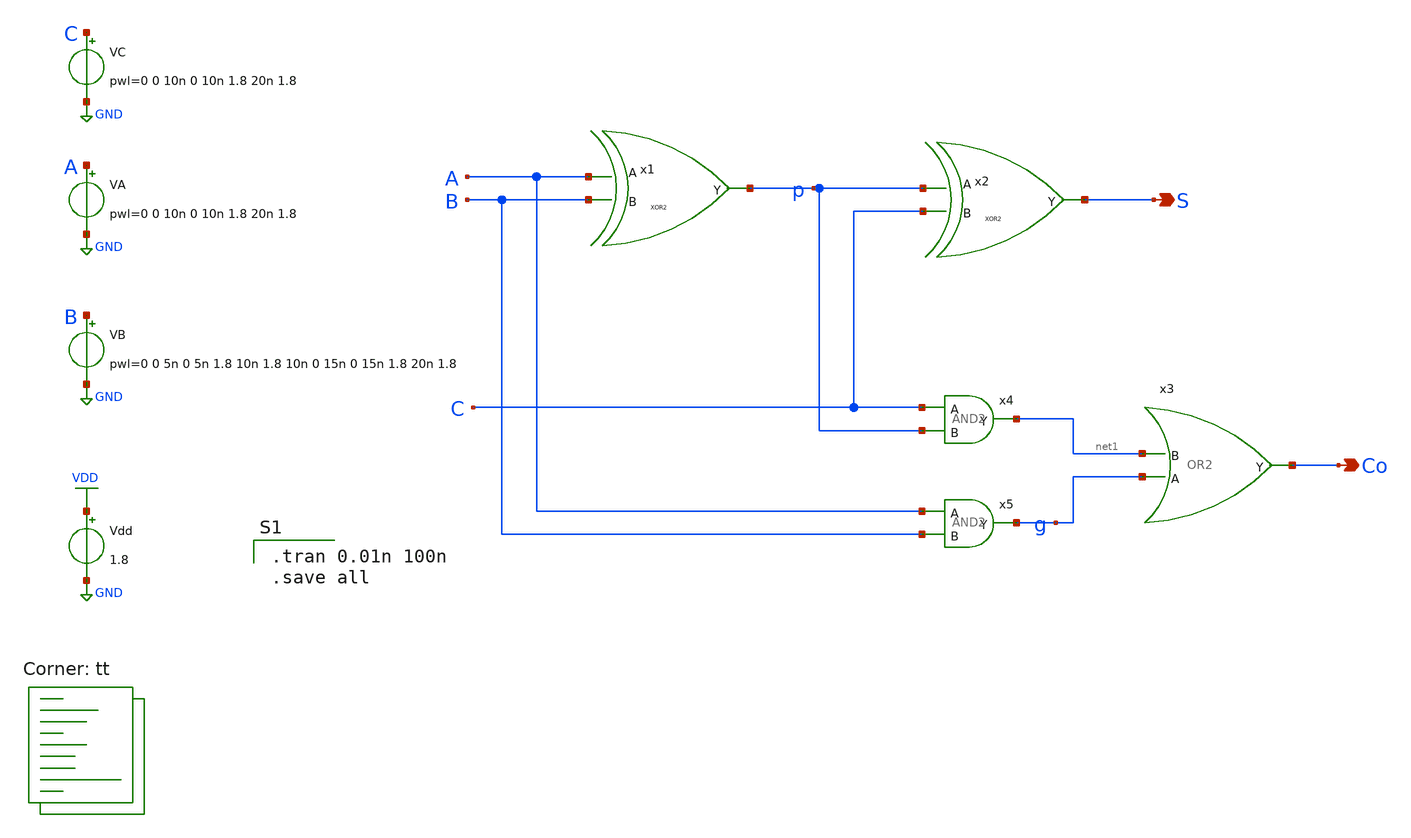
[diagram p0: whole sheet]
** sch_path: gates/FASIM.sch
**.subckt FASIM S Co
*.opin S
*.opin Co
x1 A B p XOR2
x2 p C S XOR2
x3 net1 Co g OR2
x4 C net1 p AND2
x5 A g B AND2
Vdd VDD GND 1.8
VA A GND pwl=0 0 10n 0 10n 1.8 20n 1.8
VB B GND pwl=0 0 5n 0 5n 1.8 10n 1.8 10n 0 15n 0 15n 1.8 20n 1.8
VC C GND pwl=0 0 10n 0 10n 1.8 20n 1.8
**** begin user architecture code

.tran 0.01n 100n
.save all

.lib $::SKYWATER_MODELS/sky130.lib.spice tt
**** end user architecture code
**.ends

* expanding   symbol:  XOR2.sym # of pins=3
** sym_path: gates/XOR2.sym
** sch_path: gates/XOR2.sch
.subckt XOR2 B A Y
*.ipin A
*.ipin B
*.opin Y
XM1 Y A net5 GND sky130_fd_pr__nfet_01v8 L=0.15 W=1 nf=1 ad='int((nf+1)/2) * W/nf * 0.29' as='int((nf+2)/2) * W/nf * 0.29'
+ pd='2*int((nf+1)/2) * (W/nf + 0.29)' ps='2*int((nf+2)/2) * (W/nf + 0.29)' nrd='0.29 / W' nrs='0.29 / W'
+ sa=0 sb=0 sd=0 mult=1 m=1
XM2 net5 B GND GND sky130_fd_pr__nfet_01v8 L=0.15 W=1 nf=1 ad='int((nf+1)/2) * W/nf * 0.29' as='int((nf+2)/2) * W/nf * 0.29'
+ pd='2*int((nf+1)/2) * (W/nf + 0.29)' ps='2*int((nf+2)/2) * (W/nf + 0.29)' nrd='0.29 / W' nrs='0.29 / W'
+ sa=0 sb=0 sd=0 mult=1 m=1
XM3 Y net1 net2 VDD sky130_fd_pr__pfet_01v8 L=0.15 W=1 nf=1 ad='int((nf+1)/2) * W/nf * 0.29' as='int((nf+2)/2) * W/nf * 0.29'
+ pd='2*int((nf+1)/2) * (W/nf + 0.29)' ps='2*int((nf+2)/2) * (W/nf + 0.29)' nrd='0.29 / W' nrs='0.29 / W'
+ sa=0 sb=0 sd=0 mult=1 m=1
XM4 net2 A VDD VDD sky130_fd_pr__pfet_01v8 L=0.15 W=1 nf=1 ad='int((nf+1)/2) * W/nf * 0.29' as='int((nf+2)/2) * W/nf * 0.29'
+ pd='2*int((nf+1)/2) * (W/nf + 0.29)' ps='2*int((nf+2)/2) * (W/nf + 0.29)' nrd='0.29 / W' nrs='0.29 / W'
+ sa=0 sb=0 sd=0 mult=1 m=1
XM5 net2 B VDD VDD sky130_fd_pr__pfet_01v8 L=0.15 W=1 nf=1 ad='int((nf+1)/2) * W/nf * 0.29' as='int((nf+2)/2) * W/nf * 0.29'
+ pd='2*int((nf+1)/2) * (W/nf + 0.29)' ps='2*int((nf+2)/2) * (W/nf + 0.29)' nrd='0.29 / W' nrs='0.29 / W'
+ sa=0 sb=0 sd=0 mult=1 m=1
XM6 Y net3 net2 VDD sky130_fd_pr__pfet_01v8 L=0.15 W=1 nf=1 ad='int((nf+1)/2) * W/nf * 0.29' as='int((nf+2)/2) * W/nf * 0.29'
+ pd='2*int((nf+1)/2) * (W/nf + 0.29)' ps='2*int((nf+2)/2) * (W/nf + 0.29)' nrd='0.29 / W' nrs='0.29 / W'
+ sa=0 sb=0 sd=0 mult=1 m=1
XM7 Y net1 net4 GND sky130_fd_pr__nfet_01v8 L=0.15 W=1 nf=1 ad='int((nf+1)/2) * W/nf * 0.29' as='int((nf+2)/2) * W/nf * 0.29'
+ pd='2*int((nf+1)/2) * (W/nf + 0.29)' ps='2*int((nf+2)/2) * (W/nf + 0.29)' nrd='0.29 / W' nrs='0.29 / W'
+ sa=0 sb=0 sd=0 mult=1 m=1
XM8 net4 net3 GND GND sky130_fd_pr__nfet_01v8 L=0.15 W=1 nf=1 ad='int((nf+1)/2) * W/nf * 0.29' as='int((nf+2)/2) * W/nf * 0.29'
+ pd='2*int((nf+1)/2) * (W/nf + 0.29)' ps='2*int((nf+2)/2) * (W/nf + 0.29)' nrd='0.29 / W' nrs='0.29 / W'
+ sa=0 sb=0 sd=0 mult=1 m=1
X1 A net1 inv_vtc
X2 B net3 inv_vtc
.ends


* expanding   symbol:  OR2.sym # of pins=3
** sym_path: gates/OR2.sym
** sch_path: gates/OR2.sch
.subckt OR2 B Y A
*.ipin A
*.ipin B
*.opin Y
XM7 VDD B net2 VDD sky130_fd_pr__pfet_01v8 L=0.15 W=1 nf=1 ad='int((nf+1)/2) * W/nf * 0.29' as='int((nf+2)/2) * W/nf * 0.29'
+ pd='2*int((nf+1)/2) * (W/nf + 0.29)' ps='2*int((nf+2)/2) * (W/nf + 0.29)' nrd='0.29 / W' nrs='0.29 / W'
+ sa=0 sb=0 sd=0 mult=1 m=1
XM8 GND B net1 GND sky130_fd_pr__nfet_01v8 L=0.15 W=1 nf=1 ad='int((nf+1)/2) * W/nf * 0.29' as='int((nf+2)/2) * W/nf * 0.29'
+ pd='2*int((nf+1)/2) * (W/nf + 0.29)' ps='2*int((nf+2)/2) * (W/nf + 0.29)' nrd='0.29 / W' nrs='0.29 / W'
+ sa=0 sb=0 sd=0 mult=1 m=1
XM9 net2 A net1 VDD sky130_fd_pr__pfet_01v8 L=0.15 W=1 nf=1 ad='int((nf+1)/2) * W/nf * 0.29' as='int((nf+2)/2) * W/nf * 0.29'
+ pd='2*int((nf+1)/2) * (W/nf + 0.29)' ps='2*int((nf+2)/2) * (W/nf + 0.29)' nrd='0.29 / W' nrs='0.29 / W'
+ sa=0 sb=0 sd=0 mult=1 m=1
XM10 GND A net1 GND sky130_fd_pr__nfet_01v8 L=0.15 W=1 nf=1 ad='int((nf+1)/2) * W/nf * 0.29' as='int((nf+2)/2) * W/nf * 0.29'
+ pd='2*int((nf+1)/2) * (W/nf + 0.29)' ps='2*int((nf+2)/2) * (W/nf + 0.29)' nrd='0.29 / W' nrs='0.29 / W'
+ sa=0 sb=0 sd=0 mult=1 m=1
X1 net1 Y inv_vtc
.ends


* expanding   symbol:  AND2.sym # of pins=3
** sym_path: gates/AND2.sym
** sch_path: gates/AND2.sch
.subckt AND2 A Y B
*.opin Y
*.ipin A
*.ipin B
x1 A net1 B NAND2_Gate
X2 net1 Y inv_vtc
.ends


* expanding   symbol:  inv_vtc.sym # of pins=2
** sym_path: gates/inv_vtc.sym
** sch_path: gates/inv_vtc.sch
.subckt inv_vtc A Y
*.ipin A
*.opin Y
XM1 Y A VDD VDD sky130_fd_pr__pfet_01v8 L=0.15 W=2 nf=1 ad='int((nf+1)/2) * W/nf * 0.29' as='int((nf+2)/2) * W/nf * 0.29'
+ pd='2*int((nf+1)/2) * (W/nf + 0.29)' ps='2*int((nf+2)/2) * (W/nf + 0.29)' nrd='0.29 / W' nrs='0.29 / W'
+ sa=0 sb=0 sd=0 mult=1 m=1
XM2 Y A GND GND sky130_fd_pr__nfet_01v8 L=0.15 W=1 nf=1 ad='int((nf+1)/2) * W/nf * 0.29' as='int((nf+2)/2) * W/nf * 0.29'
+ pd='2*int((nf+1)/2) * (W/nf + 0.29)' ps='2*int((nf+2)/2) * (W/nf + 0.29)' nrd='0.29 / W' nrs='0.29 / W'
+ sa=0 sb=0 sd=0 mult=1 m=1
.ends


* expanding   symbol:  NAND2_Gate.sym # of pins=3
** sym_path: gates/NAND2_Gate.sym
** sch_path: gates/NAND2_Gate.sch
.subckt NAND2_Gate A Y B
*.ipin A
*.ipin B
*.opin Y
XM1 Y A net1 GND sky130_fd_pr__nfet_01v8 L=0.15 W=1 nf=1 ad='int((nf+1)/2) * W/nf * 0.29' as='int((nf+2)/2) * W/nf * 0.29'
+ pd='2*int((nf+1)/2) * (W/nf + 0.29)' ps='2*int((nf+2)/2) * (W/nf + 0.29)' nrd='0.29 / W' nrs='0.29 / W'
+ sa=0 sb=0 sd=0 mult=1 m=1
XM2 net1 B GND GND sky130_fd_pr__nfet_01v8 L=0.15 W=1 nf=1 ad='int((nf+1)/2) * W/nf * 0.29' as='int((nf+2)/2) * W/nf * 0.29'
+ pd='2*int((nf+1)/2) * (W/nf + 0.29)' ps='2*int((nf+2)/2) * (W/nf + 0.29)' nrd='0.29 / W' nrs='0.29 / W'
+ sa=0 sb=0 sd=0 mult=1 m=1
XM3 Y A VDD VDD sky130_fd_pr__pfet_01v8 L=0.15 W=1 nf=1 ad='int((nf+1)/2) * W/nf * 0.29' as='int((nf+2)/2) * W/nf * 0.29'
+ pd='2*int((nf+1)/2) * (W/nf + 0.29)' ps='2*int((nf+2)/2) * (W/nf + 0.29)' nrd='0.29 / W' nrs='0.29 / W'
+ sa=0 sb=0 sd=0 mult=1 m=1
XM4 Y B VDD VDD sky130_fd_pr__pfet_01v8 L=0.15 W=1 nf=1 ad='int((nf+1)/2) * W/nf * 0.29' as='int((nf+2)/2) * W/nf * 0.29'
+ pd='2*int((nf+1)/2) * (W/nf + 0.29)' ps='2*int((nf+2)/2) * (W/nf + 0.29)' nrd='0.29 / W' nrs='0.29 / W'
+ sa=0 sb=0 sd=0 mult=1 m=1
.ends

.GLOBAL VDD
.GLOBAL GND
.end
